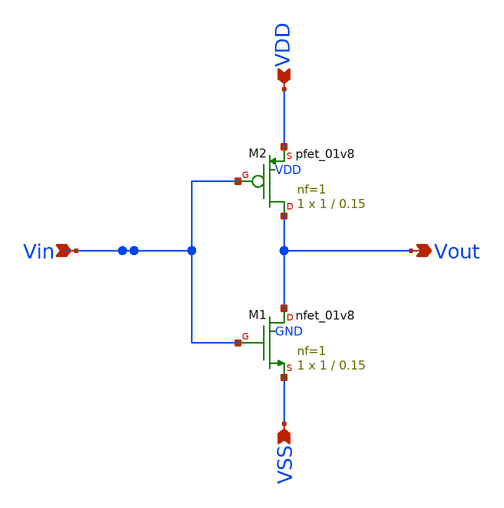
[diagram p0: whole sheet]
** sch_path: 2_bit_current_steering_DAC/inverter.sch
**.subckt inverter VDD Vin VSS Vout
*.ipin VDD
*.ipin Vin
*.ipin VSS
*.opin Vout
XM1 Vout Vin VSS GND sky130_fd_pr__nfet_01v8 L=0.15 W=1 nf=1 ad='int((1 + 1)/2) * 1 / 1 * 0.29' as='int((1 + 2)/2) * 1 / 1 * 0.29'
+ pd='2*int((1 + 1)/2) * (1 / 1 + 0.29)' ps='2*int((1 + 2)/2) * (1 / 1 + 0.29)' nrd='0.29 / 1 ' nrs='0.29 / 1 '
+ sa=0 sb=0 sd=0 mult=1 m=1
XM2 Vout Vin VDD VDD sky130_fd_pr__pfet_01v8 L=0.15 W=1 nf=1 ad='int((1 + 1)/2) * 1 / 1 * 0.29' as='int((1 + 2)/2) * 1 / 1 * 0.29'
+ pd='2*int((1 + 1)/2) * (1 / 1 + 0.29)' ps='2*int((1 + 2)/2) * (1 / 1 + 0.29)' nrd='0.29 / 1 ' nrs='0.29 / 1 '
+ sa=0 sb=0 sd=0 mult=1 m=1
**.ends
.end
